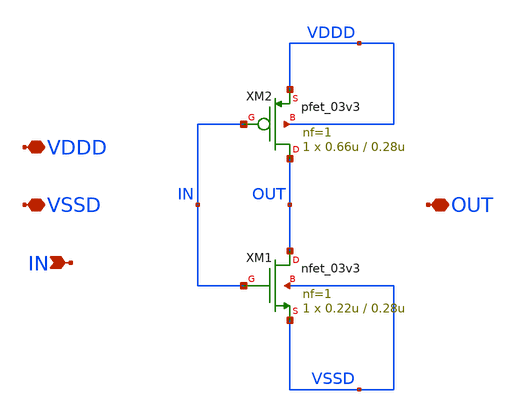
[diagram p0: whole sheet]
** sch_path: SAR_ADC/blocks/Dynamic_Comparator/Dynamic_Comparator_inv_1x.sch
**.subckt Dynamic_Comparator_inv_1x VDDD VSSD IN OUT
*.iopin VDDD
*.iopin VSSD
*.ipin IN
*.iopin OUT
XM1 OUT IN VSSD VSSD nfet_03v3 L=0.28u W=0.22u nf=1 ad='int((nf+1)/2) * W/nf * 0.18u' as='int((nf+2)/2) * W/nf * 0.18u'
+ pd='2*int((nf+1)/2) * (W/nf + 0.18u)' ps='2*int((nf+2)/2) * (W/nf + 0.18u)' nrd='0.18u / W' nrs='0.18u / W'
+ sa=0 sb=0 sd=0 m=1
XM2 OUT IN VDDD VDDD pfet_03v3 L=0.28u W=0.66u nf=1 ad='int((nf+1)/2) * W/nf * 0.18u' as='int((nf+2)/2) * W/nf * 0.18u'
+ pd='2*int((nf+1)/2) * (W/nf + 0.18u)' ps='2*int((nf+2)/2) * (W/nf + 0.18u)' nrd='0.18u / W' nrs='0.18u / W'
+ sa=0 sb=0 sd=0 m=1
**.ends
.end
